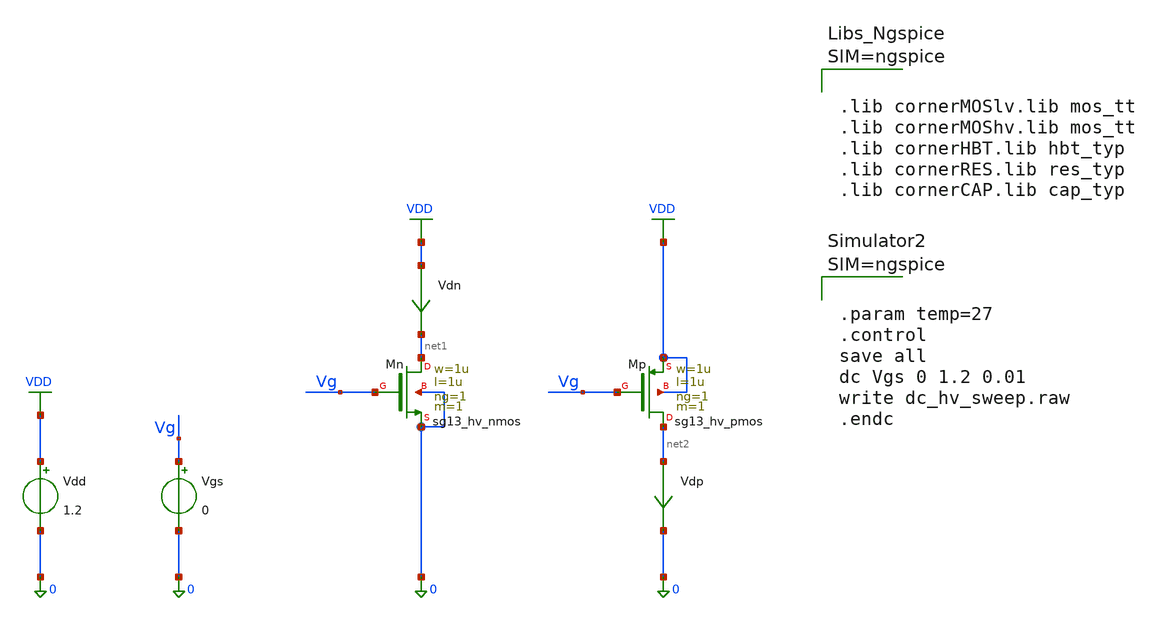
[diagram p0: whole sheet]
** sch_path: xschem/ncs-dpi-adexp/xschem/tb_mos_test.sch
**.subckt tb_mos_test
XMn net1 Vg 0 0 sg13_hv_nmos w=1u l=1u ng=1 m=1 mm_ok=1
Vdn VDD net1 0
.save i(vdn)
Vgs Vg 0 0
Vdd VDD 0 1.2
Vdp net2 0 0
.save i(vdp)
XMp net2 Vg VDD VDD sg13_hv_pmos w=1u l=1u ng=1 m=1 mm_ok=1
**** begin user architecture code



.lib cornerMOSlv.lib mos_tt
.lib cornerMOShv.lib mos_tt
.lib cornerHBT.lib hbt_typ
.lib cornerRES.lib res_typ
.lib cornerCAP.lib cap_typ






.param temp=27
.control
save all
dc Vgs 0 1.2 0.01
write dc_hv_sweep.raw
.endc



**** end user architecture code
**.ends
.GLOBAL VDD
.end
